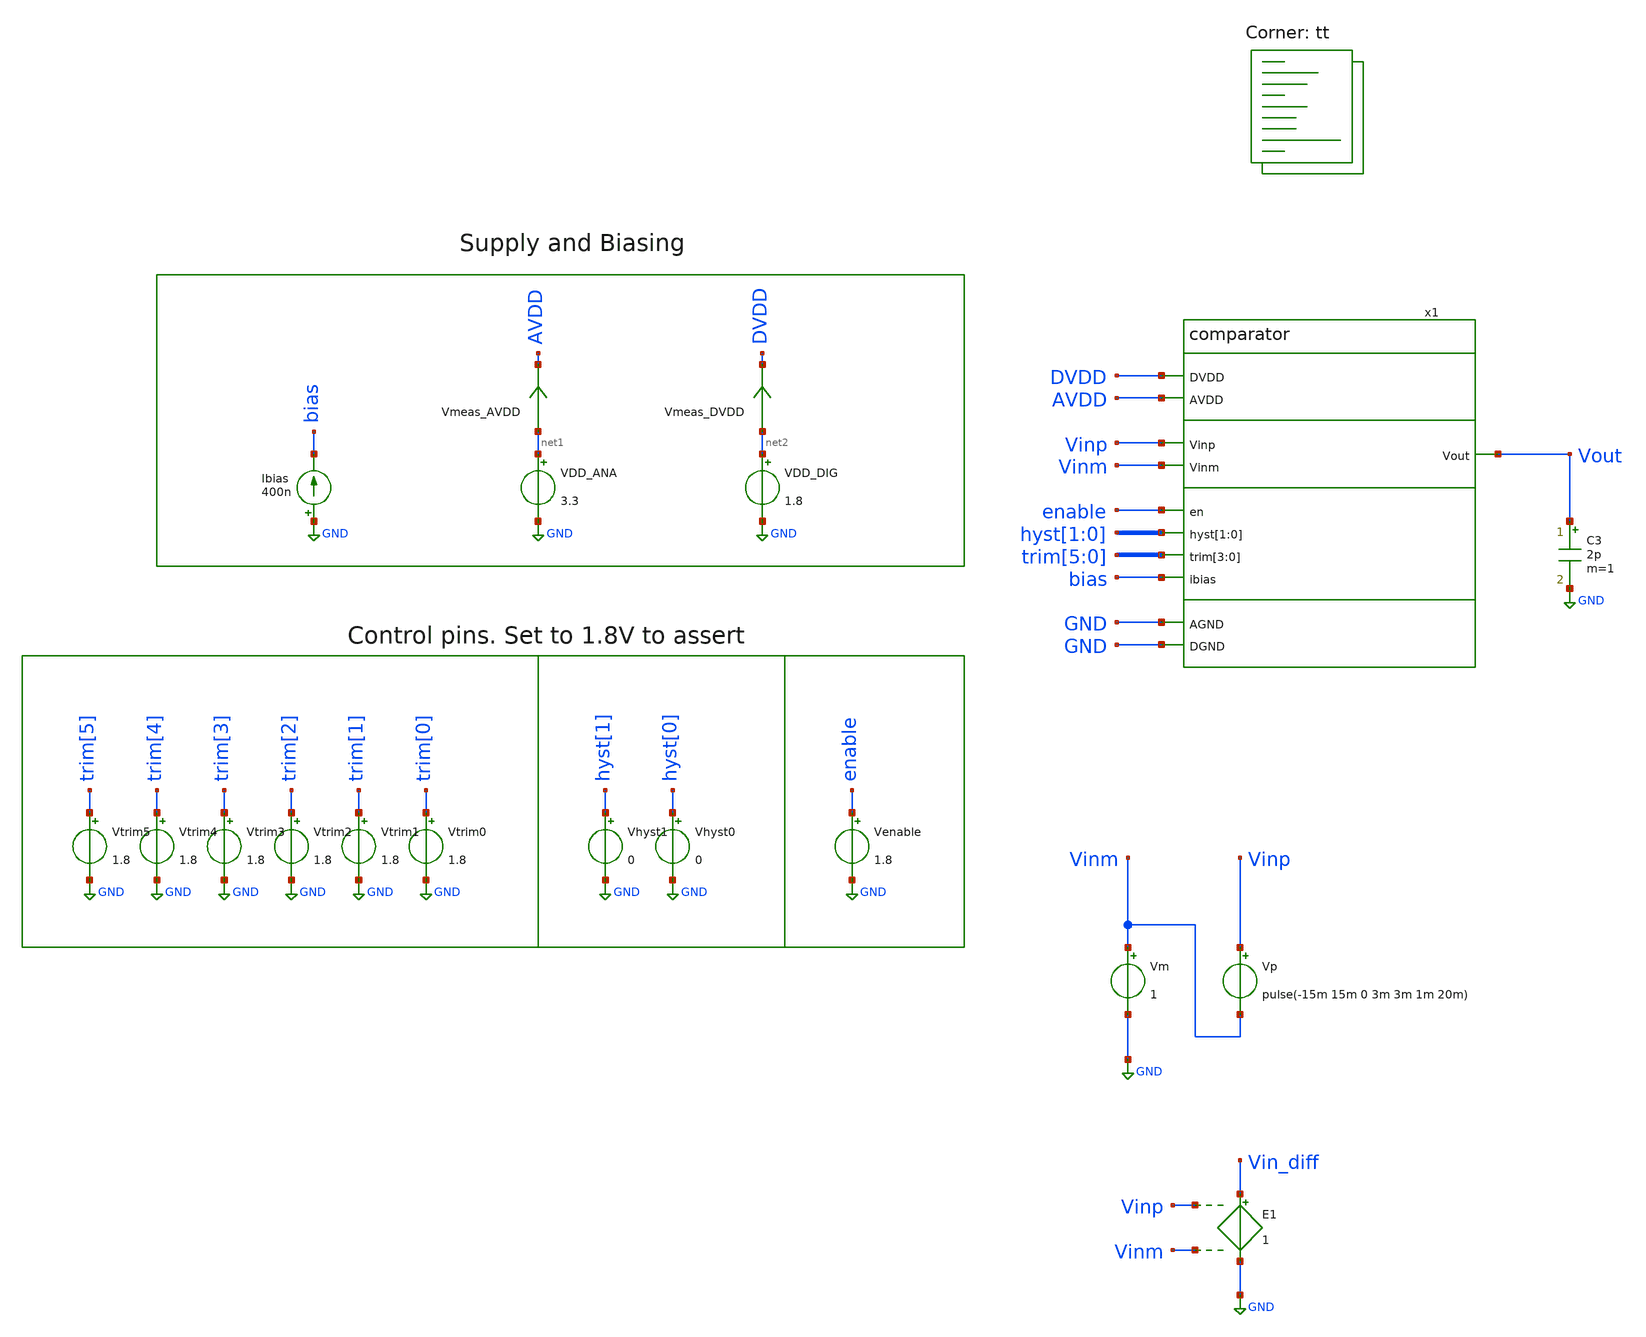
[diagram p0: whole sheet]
** sch_path: xschem/tb_comparator_trim.sch
**.subckt tb_comparator_trim
Vp Vinp Vinm pulse(-15m 15m 0 3m 3m 1m 20m)
VDD_ANA net1 GND 3.3
VDD_DIG net2 GND 1.8
Ibias GND bias 400n
C3 Vout GND 2p m=1
Vm Vinm GND 1
Vmeas_AVDD net1 AVDD 0
.save i(vmeas_avdd)
Vmeas_DVDD net2 DVDD 0
.save i(vmeas_dvdd)
E1 Vin_diff GND Vinp Vinm 1
Vtrim3 trim[3] GND 1.8
Vtrim2 trim[2] GND 1.8
Vtrim1 trim[1] GND 1.8
Vtrim0 trim[0] GND 1.8
Vhyst1 hyst[1] GND 0
Vhyst0 hyst[0] GND 0
Venable enable GND 1.8
Vtrim5 trim[5] GND 1.8
Vtrim4 trim[4] GND 1.8
x1 DVDD AVDD GND GND Vinp Vout Vinm enable hyst[1] hyst[0] trim[5] trim[4] trim[3] trim[2] bias
+ comparator
**** begin user architecture code
.lib $::SKYWATER_MODELS/sky130.lib.spice tt


.save v(vout) v(vin_diff)
*.save all
.tran 1u 3m 500u
.ic v(x1.vop)=0 v(x1.vdiff)=1.8 v(x1.vout_int)=0 v(x1.voutb)=1.8 v(vout)=0 v(x1.trim0_hv)=0
+  v(x1.trim1_hv)=0 v(x1.trim2_hv)=0 v(x1.trim3_hv)=0 v(x1.trim4_hv)=0 v(x1.trim5_hv)=0  v(x1.hyst1_hv)=0
+ v(x1.hyst0_hv)=0 v(x1.enb_hv)=0

.control
let vec=unitvec(1)
let num_meas=9
let i=0
let input_offset=unitvec(num_meas)
foreach temp_val -40 27 85
   foreach vdd_ana_val 2.95 3.3 5.5
      *foreach vm_val {$vdd_ana_val/2} {-0.01 + $vdd_ana_val}
      foreach vm_val 0.01
         foreach ibias_val 400n
            set temp=$temp_val
            alter VDD_ANA $vdd_ana_val
            alter Vm $vm_val
            alter ibias $ibias_val
            run
            meas tran t_cross when v(vout)=0.9 rise=1
            meas tran in_cross find v(vin_diff) at=t_cross
            let input_offset[i]=in_cross
            let i=i+1
            set filetype=ascii
            set appendwrite
            set wr_singlescale
            setscale vec
            wrdata results_trim_pmos_max.out in_cross
         end
      end
   end
end
*setscale time
*plot tran1.v(vout) tran2.v(vout) tran3.v(vout) tran4.v(vout) tran5.v(vout) tran6.v(vout)
*+ tran7.v(vout) tran8.v(vout) tran9.v(vout)
*print vecmin(input_offset)
*print vecmax(input_offset)
.endc


**** end user architecture code
**.ends
.GLOBAL GND
.end
